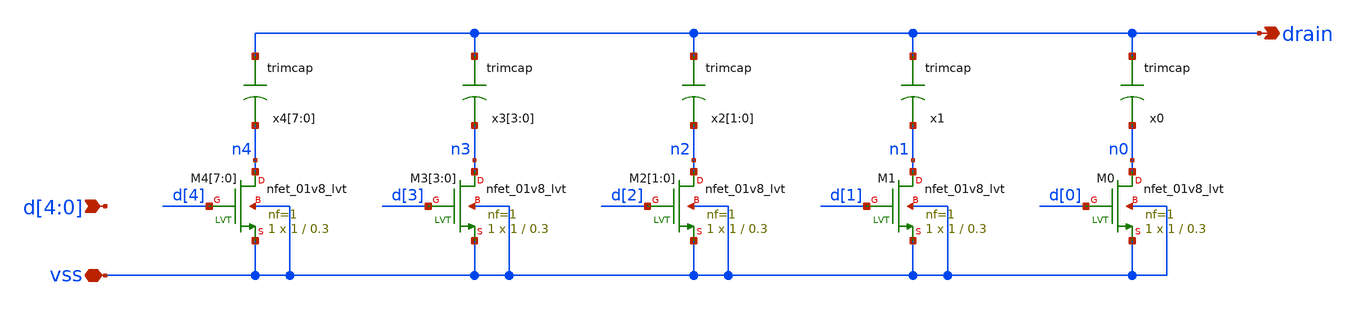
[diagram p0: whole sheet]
** sch_path: xschem/sar_10b/comparator/trim.sch
**.subckt trim vss d[4],d[3],d[2],d[1],d[0] drain
*.iopin vss
*.ipin d[4],d[3],d[2],d[1],d[0]
*.opin drain
XM4[7] n4 d[4] vss vss sky130_fd_pr__nfet_01v8_lvt L=0.3 W=1 nf=1 ad='int((nf+1)/2) * W/nf * 0.29' as='int((nf+2)/2) * W/nf * 0.29'
+ pd='2*int((nf+1)/2) * (W/nf + 0.29)' ps='2*int((nf+2)/2) * (W/nf + 0.29)' nrd='0.29 / W' nrs='0.29 / W'
+ sa=0 sb=0 sd=0 mult=1 m=1
XM4[6] n4 d[4] vss vss sky130_fd_pr__nfet_01v8_lvt L=0.3 W=1 nf=1 ad='int((nf+1)/2) * W/nf * 0.29' as='int((nf+2)/2) * W/nf * 0.29'
+ pd='2*int((nf+1)/2) * (W/nf + 0.29)' ps='2*int((nf+2)/2) * (W/nf + 0.29)' nrd='0.29 / W' nrs='0.29 / W'
+ sa=0 sb=0 sd=0 mult=1 m=1
XM4[5] n4 d[4] vss vss sky130_fd_pr__nfet_01v8_lvt L=0.3 W=1 nf=1 ad='int((nf+1)/2) * W/nf * 0.29' as='int((nf+2)/2) * W/nf * 0.29'
+ pd='2*int((nf+1)/2) * (W/nf + 0.29)' ps='2*int((nf+2)/2) * (W/nf + 0.29)' nrd='0.29 / W' nrs='0.29 / W'
+ sa=0 sb=0 sd=0 mult=1 m=1
XM4[4] n4 d[4] vss vss sky130_fd_pr__nfet_01v8_lvt L=0.3 W=1 nf=1 ad='int((nf+1)/2) * W/nf * 0.29' as='int((nf+2)/2) * W/nf * 0.29'
+ pd='2*int((nf+1)/2) * (W/nf + 0.29)' ps='2*int((nf+2)/2) * (W/nf + 0.29)' nrd='0.29 / W' nrs='0.29 / W'
+ sa=0 sb=0 sd=0 mult=1 m=1
XM4[3] n4 d[4] vss vss sky130_fd_pr__nfet_01v8_lvt L=0.3 W=1 nf=1 ad='int((nf+1)/2) * W/nf * 0.29' as='int((nf+2)/2) * W/nf * 0.29'
+ pd='2*int((nf+1)/2) * (W/nf + 0.29)' ps='2*int((nf+2)/2) * (W/nf + 0.29)' nrd='0.29 / W' nrs='0.29 / W'
+ sa=0 sb=0 sd=0 mult=1 m=1
XM4[2] n4 d[4] vss vss sky130_fd_pr__nfet_01v8_lvt L=0.3 W=1 nf=1 ad='int((nf+1)/2) * W/nf * 0.29' as='int((nf+2)/2) * W/nf * 0.29'
+ pd='2*int((nf+1)/2) * (W/nf + 0.29)' ps='2*int((nf+2)/2) * (W/nf + 0.29)' nrd='0.29 / W' nrs='0.29 / W'
+ sa=0 sb=0 sd=0 mult=1 m=1
XM4[1] n4 d[4] vss vss sky130_fd_pr__nfet_01v8_lvt L=0.3 W=1 nf=1 ad='int((nf+1)/2) * W/nf * 0.29' as='int((nf+2)/2) * W/nf * 0.29'
+ pd='2*int((nf+1)/2) * (W/nf + 0.29)' ps='2*int((nf+2)/2) * (W/nf + 0.29)' nrd='0.29 / W' nrs='0.29 / W'
+ sa=0 sb=0 sd=0 mult=1 m=1
XM4[0] n4 d[4] vss vss sky130_fd_pr__nfet_01v8_lvt L=0.3 W=1 nf=1 ad='int((nf+1)/2) * W/nf * 0.29' as='int((nf+2)/2) * W/nf * 0.29'
+ pd='2*int((nf+1)/2) * (W/nf + 0.29)' ps='2*int((nf+2)/2) * (W/nf + 0.29)' nrd='0.29 / W' nrs='0.29 / W'
+ sa=0 sb=0 sd=0 mult=1 m=1
XM3[3] n3 d[3] vss vss sky130_fd_pr__nfet_01v8_lvt L=0.3 W=1 nf=1 ad='int((nf+1)/2) * W/nf * 0.29' as='int((nf+2)/2) * W/nf * 0.29'
+ pd='2*int((nf+1)/2) * (W/nf + 0.29)' ps='2*int((nf+2)/2) * (W/nf + 0.29)' nrd='0.29 / W' nrs='0.29 / W'
+ sa=0 sb=0 sd=0 mult=1 m=1
XM3[2] n3 d[3] vss vss sky130_fd_pr__nfet_01v8_lvt L=0.3 W=1 nf=1 ad='int((nf+1)/2) * W/nf * 0.29' as='int((nf+2)/2) * W/nf * 0.29'
+ pd='2*int((nf+1)/2) * (W/nf + 0.29)' ps='2*int((nf+2)/2) * (W/nf + 0.29)' nrd='0.29 / W' nrs='0.29 / W'
+ sa=0 sb=0 sd=0 mult=1 m=1
XM3[1] n3 d[3] vss vss sky130_fd_pr__nfet_01v8_lvt L=0.3 W=1 nf=1 ad='int((nf+1)/2) * W/nf * 0.29' as='int((nf+2)/2) * W/nf * 0.29'
+ pd='2*int((nf+1)/2) * (W/nf + 0.29)' ps='2*int((nf+2)/2) * (W/nf + 0.29)' nrd='0.29 / W' nrs='0.29 / W'
+ sa=0 sb=0 sd=0 mult=1 m=1
XM3[0] n3 d[3] vss vss sky130_fd_pr__nfet_01v8_lvt L=0.3 W=1 nf=1 ad='int((nf+1)/2) * W/nf * 0.29' as='int((nf+2)/2) * W/nf * 0.29'
+ pd='2*int((nf+1)/2) * (W/nf + 0.29)' ps='2*int((nf+2)/2) * (W/nf + 0.29)' nrd='0.29 / W' nrs='0.29 / W'
+ sa=0 sb=0 sd=0 mult=1 m=1
XM2[1] n2 d[2] vss vss sky130_fd_pr__nfet_01v8_lvt L=0.3 W=1 nf=1 ad='int((nf+1)/2) * W/nf * 0.29' as='int((nf+2)/2) * W/nf * 0.29'
+ pd='2*int((nf+1)/2) * (W/nf + 0.29)' ps='2*int((nf+2)/2) * (W/nf + 0.29)' nrd='0.29 / W' nrs='0.29 / W'
+ sa=0 sb=0 sd=0 mult=1 m=1
XM2[0] n2 d[2] vss vss sky130_fd_pr__nfet_01v8_lvt L=0.3 W=1 nf=1 ad='int((nf+1)/2) * W/nf * 0.29' as='int((nf+2)/2) * W/nf * 0.29'
+ pd='2*int((nf+1)/2) * (W/nf + 0.29)' ps='2*int((nf+2)/2) * (W/nf + 0.29)' nrd='0.29 / W' nrs='0.29 / W'
+ sa=0 sb=0 sd=0 mult=1 m=1
XM1 n1 d[1] vss vss sky130_fd_pr__nfet_01v8_lvt L=0.3 W=1 nf=1 ad='int((nf+1)/2) * W/nf * 0.29' as='int((nf+2)/2) * W/nf * 0.29'
+ pd='2*int((nf+1)/2) * (W/nf + 0.29)' ps='2*int((nf+2)/2) * (W/nf + 0.29)' nrd='0.29 / W' nrs='0.29 / W'
+ sa=0 sb=0 sd=0 mult=1 m=1
XM0 n0 d[0] vss vss sky130_fd_pr__nfet_01v8_lvt L=0.3 W=1 nf=1 ad='int((nf+1)/2) * W/nf * 0.29' as='int((nf+2)/2) * W/nf * 0.29'
+ pd='2*int((nf+1)/2) * (W/nf + 0.29)' ps='2*int((nf+2)/2) * (W/nf + 0.29)' nrd='0.29 / W' nrs='0.29 / W'
+ sa=0 sb=0 sd=0 mult=1 m=1
x4[7] drain n4 trimcap
x4[6] drain n4 trimcap
x4[5] drain n4 trimcap
x4[4] drain n4 trimcap
x4[3] drain n4 trimcap
x4[2] drain n4 trimcap
x4[1] drain n4 trimcap
x4[0] drain n4 trimcap
x3[3] drain n3 trimcap
x3[2] drain n3 trimcap
x3[1] drain n3 trimcap
x3[0] drain n3 trimcap
x2[1] drain n2 trimcap
x2[0] drain n2 trimcap
x1 drain n1 trimcap
x0 drain n0 trimcap
**.ends

* expanding   symbol:  sar_10b/comparator/trimcap.sym # of pins=2
** sym_path: xschem/sar_10b/comparator/trimcap.sym
** sch_path: xschem/sar_10b/comparator/trimcap.sch
.subckt trimcap cp cn
*.iopin cp
*.iopin cn
c0 net1 cn 2f m=1
c1 cp net1 1f m=1
.ends

.end
